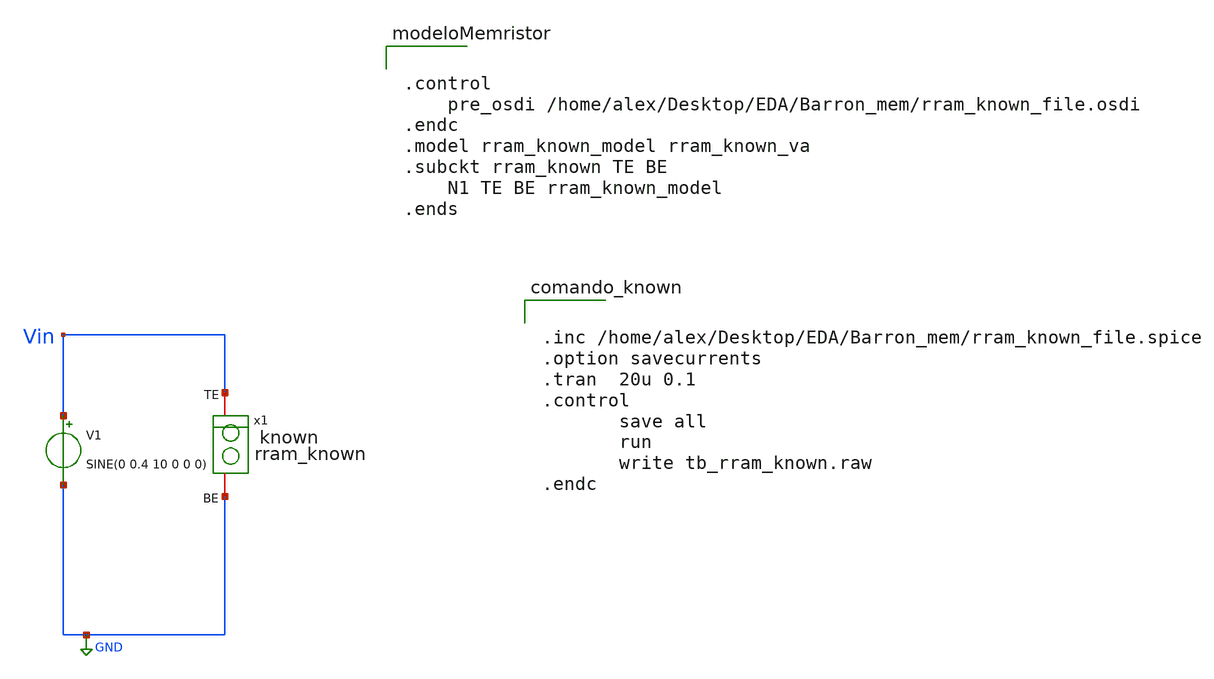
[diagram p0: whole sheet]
** sch_path: tb_rram_known.sch
**.subckt tb_rram_known
V1 Vin GND SINE(0 0.4 10 0 0 0)
Xx1 Vin GND rram_known
**** begin user architecture code


.inc /home/alex/Desktop/EDA/Barron_mem/rram_known_file.spice
.option savecurrents
.tran  20u 0.1
.control
       save all
       run
       write tb_rram_known.raw
.endc




.control
	pre_osdi /home/alex/Desktop/EDA/Barron_mem/rram_known_file.osdi
.endc
.model rram_known_model rram_known_va
.subckt rram_known TE BE
	N1 TE BE rram_known_model
.ends


**** end user architecture code
**.ends
.GLOBAL GND
.end
